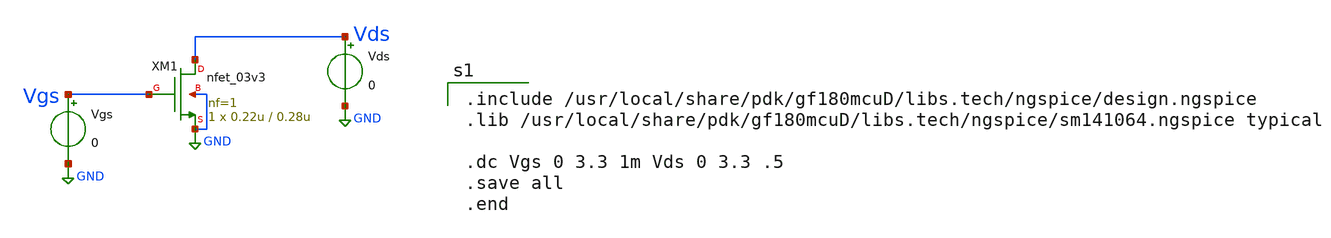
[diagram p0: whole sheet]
** sch_path: schem/dc_sweep.sch
**.subckt dc_sweep
XM1 Vds Vgs GND GND nfet_03v3 L=0.28u W=0.22u nf=1 ad='int((nf+1)/2) * W/nf * 0.18u' as='int((nf+2)/2) * W/nf * 0.18u'
+ pd='2*int((nf+1)/2) * (W/nf + 0.18u)' ps='2*int((nf+2)/2) * (W/nf + 0.18u)' nrd='0.18u / W' nrs='0.18u / W'
+ sa=0 sb=0 sd=0 m=1
Vgs Vgs GND 0
Vds Vds GND 0
**** begin user architecture code

.include /usr/local/share/pdk/gf180mcuD/libs.tech/ngspice/design.ngspice
.lib /usr/local/share/pdk/gf180mcuD/libs.tech/ngspice/sm141064.ngspice typical

.dc Vgs 0 3.3 1m Vds 0 3.3 .5
.save all
.end


**** end user architecture code
**.ends
.GLOBAL GND
.end
